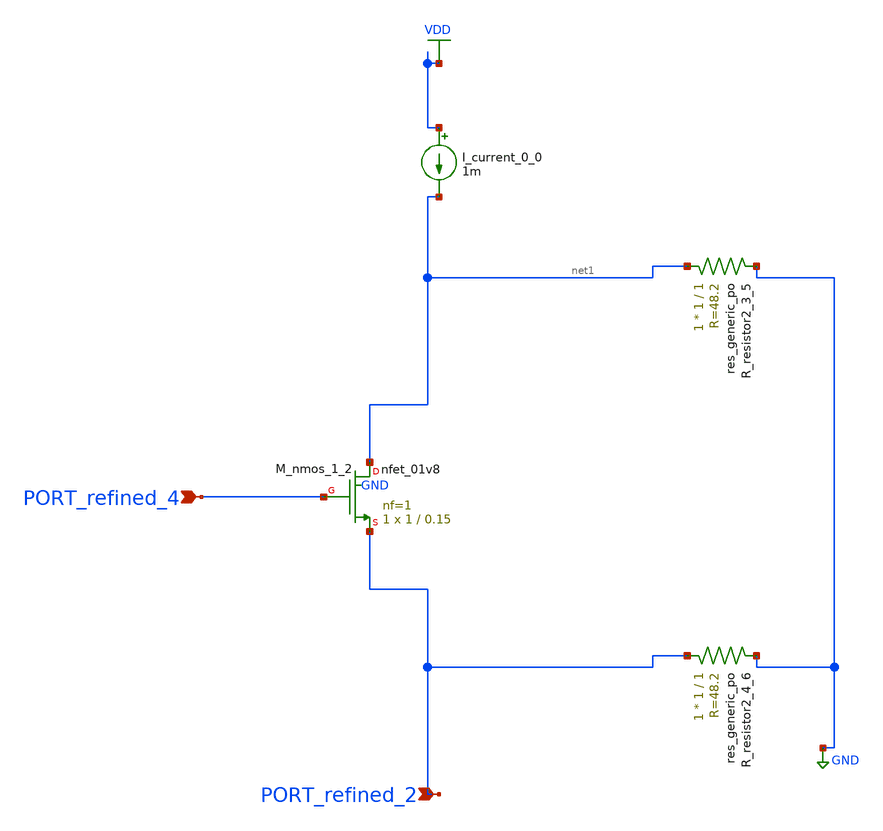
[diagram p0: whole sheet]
** sch_path: schematics/AMSNet/358.sch
**.subckt 358 PORT_refined_4 PORT_refined_2
*.ipin PORT_refined_4
*.ipin PORT_refined_2
I_current_0_0 VDD net1 1m
XM_nmos_1_2 net1 PORT_refined_4 PORT_refined_2 GND sky130_fd_pr__nfet_01v8 L=0.15 W=1 nf=1 ad='int((1 + 1)/2) * 1 / 1 * 0.29'
+ as='int((1 + 2)/2) * 1 / 1 * 0.29' pd='2*int((1 + 1)/2) * (1 / 1 + 0.29)' ps='2*int((1 + 2)/2) * (1 / 1 + 0.29)'
+ nrd='0.29 / 1 ' nrs='0.29 / 1 ' sa=0 sb=0 sd=0 mult=1 m=1
XR_resistor2_3_5 net1 GND sky130_fd_pr__res_generic_po W=1 L=1 m=1
XR_resistor2_4_6 PORT_refined_2 GND sky130_fd_pr__res_generic_po W=1 L=1 m=1
**.ends
.GLOBAL GND
.GLOBAL VDD
.end
